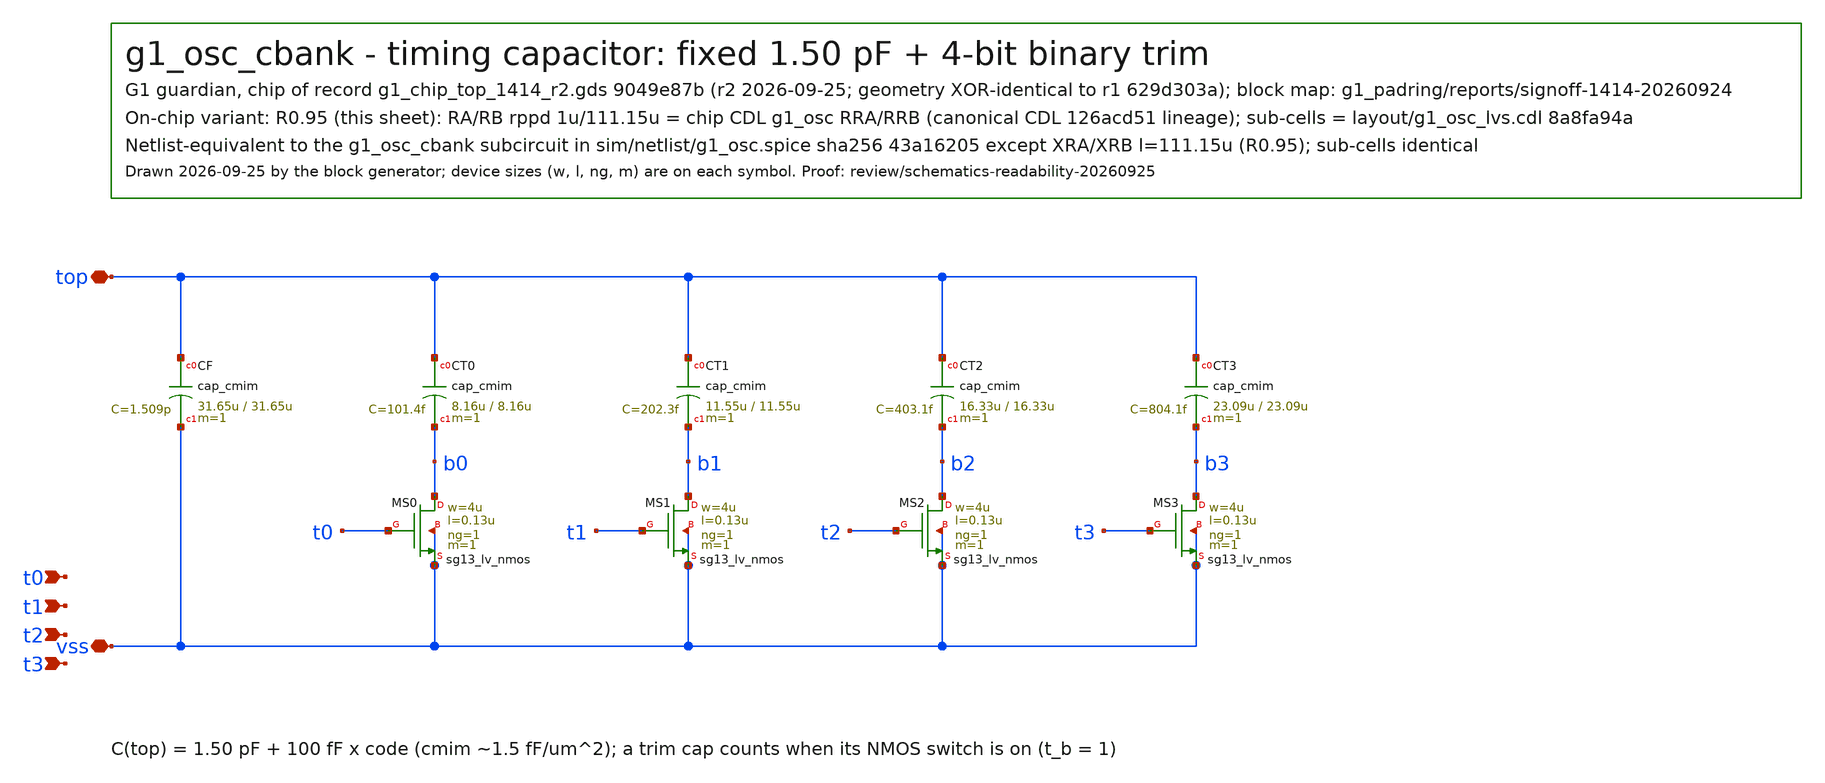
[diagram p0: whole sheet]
** sch_path: designs/g1-guardian/blocks/g1_osc/schematic/g1_osc_cbank.sch
**.subckt g1_osc_cbank t0 t1 t2 t3 top vss
*.ipin t0
*.ipin t1
*.ipin t2
*.ipin t3
*.iopin top
*.iopin vss
XCF top vss cap_cmim w=31.65u l=31.65u m=1 mm_ok=1
XCT0 top b0 cap_cmim w=8.16u l=8.16u m=1 mm_ok=1
XMS0 b0 t0 vss vss sg13_lv_nmos w=4u l=0.13u ng=1 m=1 mm_ok=1
XCT1 top b1 cap_cmim w=11.55u l=11.55u m=1 mm_ok=1
XMS1 b1 t1 vss vss sg13_lv_nmos w=4u l=0.13u ng=1 m=1 mm_ok=1
XCT2 top b2 cap_cmim w=16.33u l=16.33u m=1 mm_ok=1
XMS2 b2 t2 vss vss sg13_lv_nmos w=4u l=0.13u ng=1 m=1 mm_ok=1
XCT3 top b3 cap_cmim w=23.09u l=23.09u m=1 mm_ok=1
XMS3 b3 t3 vss vss sg13_lv_nmos w=4u l=0.13u ng=1 m=1 mm_ok=1
**.ends
.end
